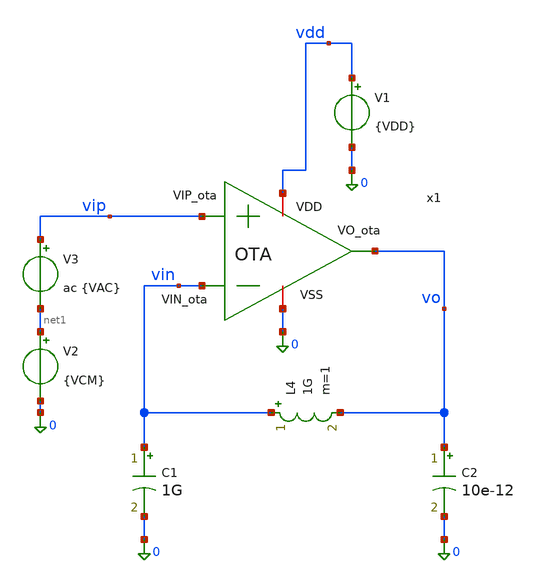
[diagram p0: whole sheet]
** sch_path: xschem/OTA_tb.sch
**.subckt OTA_tb
x1 vdd vo vin vip 0 OTA
V1 vdd 0 {VDD}
V2 net1 0 {VCM}
V3 vip net1 ac {VAC}
C1 vin 0 1G m=1
L4 vin vo 1G m=1
C2 vo 0 10e-12 m=1
**** begin user architecture code




* 1. Inclusión de libreria de modelos Sky130 PRIMERO
.lib /foss/pdks/sky130A/libs.tech/ngspice/sky130.lib.spice tt

**parametros_ota
.param VDD = 1.8
.param VCM = 0.6
.param VAC = 1



.control

save all
* PMOS
* --- Circuito de Polarización (Referencia) ---

* Mr1 (pfet_01v8_lvt)
save @m.x1.xMr1.msky130_fd_pr__pfet_01v8_lvt[gm]
save @m.x1.xMr1.msky130_fd_pr__pfet_01v8_lvt[gds]
save @m.x1.xMr1.msky130_fd_pr__pfet_01v8_lvt[id]
save @m.x1.xMr1.msky130_fd_pr__pfet_01v8_lvt[vgs]
save @m.x1.xMr1.msky130_fd_pr__pfet_01v8_lvt[vds]
save @m.x1.xMr1.msky130_fd_pr__pfet_01v8_lvt[vth]
save @m.x1.xMr1.msky130_fd_pr__pfet_01v8_lvt[vdsat]

* Mr (pfet_01v8_lvt)
save @m.x1.xMr.msky130_fd_pr__pfet_01v8_lvt[gm]
save @m.x1.xMr.msky130_fd_pr__pfet_01v8_lvt[gds]
save @m.x1.xMr.msky130_fd_pr__pfet_01v8_lvt[id]
save @m.x1.xMr.msky130_fd_pr__pfet_01v8_lvt[vgs]
save @m.x1.xMr.msky130_fd_pr__pfet_01v8_lvt[vds]
save @m.x1.xMr.msky130_fd_pr__pfet_01v8_lvt[vth]
save @m.x1.xMr.msky130_fd_pr__pfet_01v8_lvt[vdsat]

* Mp2 (nfet_01v8)
save @m.x1.xMp2.msky130_fd_pr__nfet_01v8[gm]
save @m.x1.xMp2.msky130_fd_pr__nfet_01v8[gds]
save @m.x1.xMp2.msky130_fd_pr__nfet_01v8[id]
save @m.x1.xMp2.msky130_fd_pr__nfet_01v8[vgs]
save @m.x1.xMp2.msky130_fd_pr__nfet_01v8[vds]
save @m.x1.xMp2.msky130_fd_pr__nfet_01v8[vth]
save @m.x1.xMp2.msky130_fd_pr__nfet_01v8[vdsat]

* Mc3 (nfet_01v8)
save @m.x1.xMc3.msky130_fd_pr__nfet_01v8[gm]
save @m.x1.xMc3.msky130_fd_pr__nfet_01v8[gds]
save @m.x1.xMc3.msky130_fd_pr__nfet_01v8[id]
save @m.x1.xMc3.msky130_fd_pr__nfet_01v8[vgs]
save @m.x1.xMc3.msky130_fd_pr__nfet_01v8[vds]
save @m.x1.xMc3.msky130_fd_pr__nfet_01v8[vth]
save @m.x1.xMc3.msky130_fd_pr__nfet_01v8[vdsat]


* --- Etapa Diferencial (Núcleo del OTA) ---

* Mrc1 (pfet_01v8_lvt)
save @m.x1.xMrc1.msky130_fd_pr__pfet_01v8_lvt[gm]
save @m.x1.xMrc1.msky130_fd_pr__pfet_01v8_lvt[gds]
save @m.x1.xMrc1.msky130_fd_pr__pfet_01v8_lvt[id]
save @m.x1.xMrc1.msky130_fd_pr__pfet_01v8_lvt[vgs]
save @m.x1.xMrc1.msky130_fd_pr__pfet_01v8_lvt[vds]
save @m.x1.xMrc1.msky130_fd_pr__pfet_01v8_lvt[vth]
save @m.x1.xMrc1.msky130_fd_pr__pfet_01v8_lvt[vdsat]

* Mn (pfet_01v8)
save @m.x1.xMn.msky130_fd_pr__pfet_01v8[gm]
save @m.x1.xMn.msky130_fd_pr__pfet_01v8[gds]
save @m.x1.xMn.msky130_fd_pr__pfet_01v8[id]
save @m.x1.xMn.msky130_fd_pr__pfet_01v8[vgs]
save @m.x1.xMn.msky130_fd_pr__pfet_01v8[vds]
save @m.x1.xMn.msky130_fd_pr__pfet_01v8[vth]
save @m.x1.xMn.msky130_fd_pr__pfet_01v8[vdsat]

* Mp (pfet_01v8)
save @m.x1.xMp.msky130_fd_pr__pfet_01v8[gm]
save @m.x1.xMp.msky130_fd_pr__pfet_01v8[gds]
save @m.x1.xMp.msky130_fd_pr__pfet_01v8[id]
save @m.x1.xMp.msky130_fd_pr__pfet_01v8[vgs]
save @m.x1.xMp.msky130_fd_pr__pfet_01v8[vds]
save @m.x1.xMp.msky130_fd_pr__pfet_01v8[vth]
save @m.x1.xMp.msky130_fd_pr__pfet_01v8[vdsat]

* Mnr (nfet_01v8)
save @m.x1.xMnr.msky130_fd_pr__nfet_01v8[gm]
save @m.x1.xMnr.msky130_fd_pr__nfet_01v8[gds]
save @m.x1.xMnr.msky130_fd_pr__nfet_01v8[id]
save @m.x1.xMnr.msky130_fd_pr__nfet_01v8[vgs]
save @m.x1.xMnr.msky130_fd_pr__nfet_01v8[vds]
save @m.x1.xMnr.msky130_fd_pr__nfet_01v8[vth]
save @m.x1.xMnr.msky130_fd_pr__nfet_01v8[vdsat]

* Mpr (nfet_01v8)
save @m.x1.xMpr.msky130_fd_pr__nfet_01v8[gm]
save @m.x1.xMpr.msky130_fd_pr__nfet_01v8[gds]
save @m.x1.xMpr.msky130_fd_pr__nfet_01v8[id]
save @m.x1.xMpr.msky130_fd_pr__nfet_01v8[vgs]
save @m.x1.xMpr.msky130_fd_pr__nfet_01v8[vds]
save @m.x1.xMpr.msky130_fd_pr__nfet_01v8[vth]
save @m.x1.xMpr.msky130_fd_pr__nfet_01v8[vdsat]


* --- Etapa de Salida ---

* Mrc2 (pfet_01v8_lvt)
save @m.x1.xMrc2.msky130_fd_pr__pfet_01v8_lvt[gm]
save @m.x1.xMrc2.msky130_fd_pr__pfet_01v8_lvt[gds]
save @m.x1.xMrc2.msky130_fd_pr__pfet_01v8_lvt[id]
save @m.x1.xMrc2.msky130_fd_pr__pfet_01v8_lvt[vgs]
save @m.x1.xMrc2.msky130_fd_pr__pfet_01v8_lvt[vds]
save @m.x1.xMrc2.msky130_fd_pr__pfet_01v8_lvt[vth]
save @m.x1.xMrc2.msky130_fd_pr__pfet_01v8_lvt[vdsat]

* Mo (nfet_01v8)
save @m.x1.xMo.msky130_fd_pr__nfet_01v8[gm]
save @m.x1.xMo.msky130_fd_pr__nfet_01v8[gds]
save @m.x1.xMo.msky130_fd_pr__nfet_01v8[id]
save @m.x1.xMo.msky130_fd_pr__nfet_01v8[vgs]
save @m.x1.xMo.msky130_fd_pr__nfet_01v8[vds]
save @m.x1.xMo.msky130_fd_pr__nfet_01v8[vth]
save @m.x1.xMo.msky130_fd_pr__nfet_01v8[vdsat]

set filetype=ascii
op
write OTA_op.raw


ac dec 10 1 1G
write OTA_ac.raw


* 1. Frecuencia de Corte a -3dB
meas ac f3db WHEN vdb(vo) = vdb(vo)[0] - 3

* 2. UGB (Frecuencia donde la magnitud cruza 0 dB)
meas ac ugb WHEN vdb(vo) = 0

* 3. Crear el vector de fase y convertirlo a grados (multiplicando por 180/pi)
let fase_deg = cph(v(vo)) * 180 / pi

* 4. Medir la fase en grados en el punto exacto del UGB
meas ac fase_ugb FIND fase_deg WHEN vdb(vo) = 0

* 5. Calcular el Margen de Fase automáticamente
let margen_fase = 180 + fase_ugb
print margen_fase

* 6. Graficar la magnitud y la fase ya convertida a grados
plot vdb(vo)
plot fase_deg
.endc


**** end user architecture code
**.ends

* expanding   symbol:  /foss/designs/LDO-sky130/xschem/OTA.sym # of pins=5
** sym_path: xschem/OTA.sym
** sch_path: xschem/OTA.sch
.subckt OTA VDD VO_ota VIN_ota VIP_ota VSS
*.ipin VIN_ota
*.opin VO_ota
*.iopin VSS
*.iopin VDD
*.ipin VIP_ota
XR1 VO_ota1 net1 VDD sky130_fd_pr__res_high_po W=0.35 L=360 mult=1 m=1
XC1 VO_ota net1 sky130_fd_pr__cap_mim_m3_2 W=50 L=50 MF=1 m=1
XMpr VO_ota1 vd VSS VSS sky130_fd_pr__nfet_01v8 L=0.5 W=3 nf=1 ad='int((1 + 1)/2) * 3 / 1 * 0.29' as='int((1 + 2)/2) * 3 / 1 * 0.29'
+ pd='2*int((1 + 1)/2) * (3 / 1 + 0.29)' ps='2*int((1 + 2)/2) * (3 / 1 + 0.29)' nrd='0.29 / 3 ' nrs='0.29 / 3 '
+ sa=0 sb=0 sd=0 mult=1 m=1
XMnr vd vd VSS VSS sky130_fd_pr__nfet_01v8 L=0.5 W=3 nf=1 ad='int((1 + 1)/2) * 3 / 1 * 0.29' as='int((1 + 2)/2) * 3 / 1 * 0.29'
+ pd='2*int((1 + 1)/2) * (3 / 1 + 0.29)' ps='2*int((1 + 2)/2) * (3 / 1 + 0.29)' nrd='0.29 / 3 ' nrs='0.29 / 3 '
+ sa=0 sb=0 sd=0 mult=1 m=1
XMn vd VIN_ota Vtail VDD sky130_fd_pr__pfet_01v8 L=0.5 W=28 nf=1 ad='int((1 + 1)/2) * 28 / 1 * 0.29'
+ as='int((1 + 2)/2) * 28 / 1 * 0.29' pd='2*int((1 + 1)/2) * (28 / 1 + 0.29)' ps='2*int((1 + 2)/2) * (28 / 1 + 0.29)'
+ nrd='0.29 / 28 ' nrs='0.29 / 28 ' sa=0 sb=0 sd=0 mult=1 m=1
XMp VO_ota1 VIP_ota Vtail VDD sky130_fd_pr__pfet_01v8 L=0.5 W=28 nf=1 ad='int((1 + 1)/2) * 28 / 1 * 0.29'
+ as='int((1 + 2)/2) * 28 / 1 * 0.29' pd='2*int((1 + 1)/2) * (28 / 1 + 0.29)' ps='2*int((1 + 2)/2) * (28 / 1 + 0.29)'
+ nrd='0.29 / 28 ' nrs='0.29 / 28 ' sa=0 sb=0 sd=0 mult=1 m=1
XMo VO_ota VO_ota1 VSS VSS sky130_fd_pr__nfet_01v8 L=0.5 W=3 nf=1 ad='int((1 + 1)/2) * 3 / 1 * 0.29'
+ as='int((1 + 2)/2) * 3 / 1 * 0.29' pd='2*int((1 + 1)/2) * (3 / 1 + 0.29)' ps='2*int((1 + 2)/2) * (3 / 1 + 0.29)'
+ nrd='0.29 / 3 ' nrs='0.29 / 3 ' sa=0 sb=0 sd=0 mult=1 m=1
XMrc1 Vtail VGP VDD VDD sky130_fd_pr__pfet_01v8_lvt L=0.5 W=40 nf=1 ad='int((1 + 1)/2) * 40 / 1 * 0.29'
+ as='int((1 + 2)/2) * 40 / 1 * 0.29' pd='2*int((1 + 1)/2) * (40 / 1 + 0.29)' ps='2*int((1 + 2)/2) * (40 / 1 + 0.29)'
+ nrd='0.29 / 40 ' nrs='0.29 / 40 ' sa=0 sb=0 sd=0 mult=1 m=1
XMrc2 VO_ota VGP VDD VDD sky130_fd_pr__pfet_01v8_lvt L=0.5 W=8 nf=1 ad='int((1 + 1)/2) * 8 / 1 * 0.29'
+ as='int((1 + 2)/2) * 8 / 1 * 0.29' pd='2*int((1 + 1)/2) * (8 / 1 + 0.29)' ps='2*int((1 + 2)/2) * (8 / 1 + 0.29)'
+ nrd='0.29 / 8 ' nrs='0.29 / 8 ' sa=0 sb=0 sd=0 mult=1 m=1
XMc3 VGP Viref rs VSS sky130_fd_pr__nfet_01v8 L=1 W=20 nf=1 ad='int((1 + 1)/2) * 20 / 1 * 0.29' as='int((1 + 2)/2) * 20 / 1 * 0.29'
+ pd='2*int((1 + 1)/2) * (20 / 1 + 0.29)' ps='2*int((1 + 2)/2) * (20 / 1 + 0.29)' nrd='0.29 / 20 ' nrs='0.29 / 20 '
+ sa=0 sb=0 sd=0 mult=1 m=1
XMp2 Viref Viref VSS VSS sky130_fd_pr__nfet_01v8 L=1 W=5 nf=1 ad='int((1 + 1)/2) * 5 / 1 * 0.29' as='int((1 + 2)/2) * 5 / 1 * 0.29'
+ pd='2*int((1 + 1)/2) * (5 / 1 + 0.29)' ps='2*int((1 + 2)/2) * (5 / 1 + 0.29)' nrd='0.29 / 5 ' nrs='0.29 / 5 '
+ sa=0 sb=0 sd=0 mult=1 m=1
XMr VGP VGP VDD VDD sky130_fd_pr__pfet_01v8_lvt L=0.5 W=2.4 nf=1 ad='int((1 + 1)/2) * 2.4 / 1 * 0.29'
+ as='int((1 + 2)/2) * 2.4 / 1 * 0.29' pd='2*int((1 + 1)/2) * (2.4 / 1 + 0.29)' ps='2*int((1 + 2)/2) * (2.4 / 1 + 0.29)'
+ nrd='0.29 / 2.4 ' nrs='0.29 / 2.4 ' sa=0 sb=0 sd=0 mult=1 m=1
XMr1 Viref VGP VDD VDD sky130_fd_pr__pfet_01v8_lvt L=1 W=8 nf=1 ad='int((1 + 1)/2) * 8 / 1 * 0.29' as='int((1 + 2)/2) * 8 / 1 * 0.29'
+ pd='2*int((1 + 1)/2) * (8 / 1 + 0.29)' ps='2*int((1 + 2)/2) * (8 / 1 + 0.29)' nrd='0.29 / 8 ' nrs='0.29 / 8 '
+ sa=0 sb=0 sd=0 mult=1 m=1
XRs VSS rs VSS sky130_fd_pr__res_iso_pw W=0.425 L=0.35 m=1
.ends

.end
